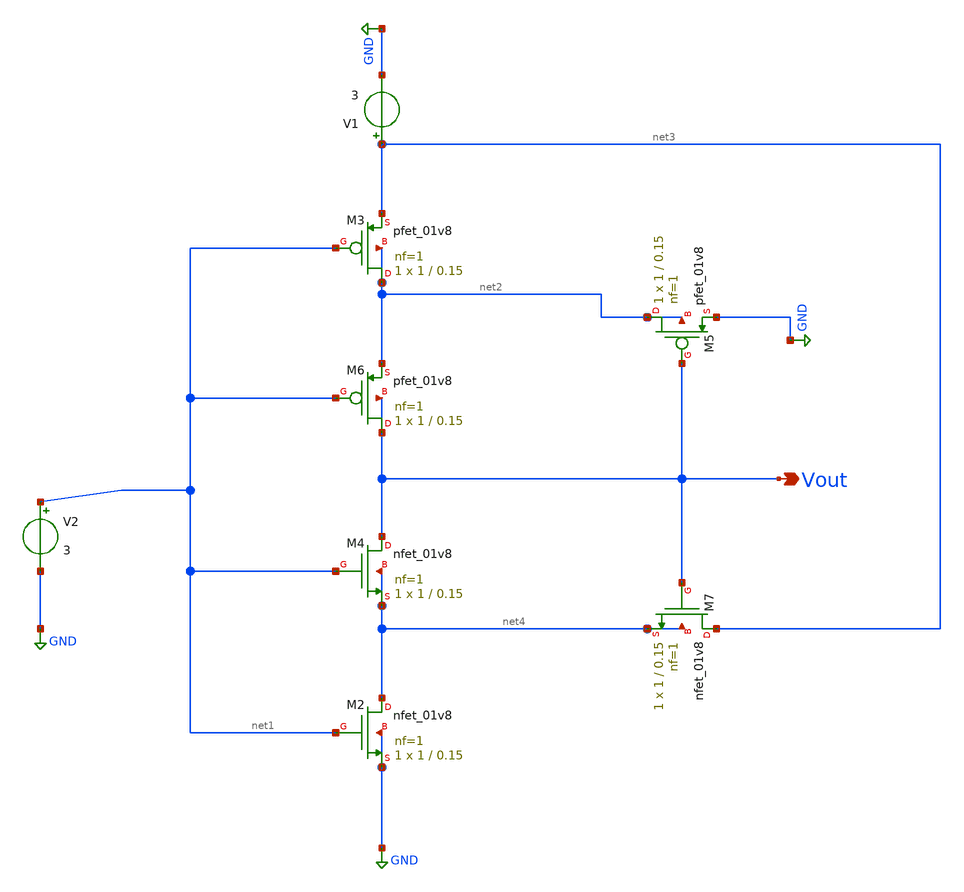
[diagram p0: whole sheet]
** sch_path: Schematics Final/Schmitt Trigger.sch
**.subckt Schmitt Trigger Vout
*.opin Vout
XM2 net4 net1 GND GND sky130_fd_pr__nfet_01v8 L=0.15 W=1 nf=1 ad='int((nf+1)/2) * W/nf * 0.29' as='int((nf+2)/2) * W/nf * 0.29'
+ pd='2*int((nf+1)/2) * (W/nf + 0.29)' ps='2*int((nf+2)/2) * (W/nf + 0.29)' nrd='0.29 / W' nrs='0.29 / W'
+ sa=0 sb=0 sd=0 mult=1 m=1
XM4 Vout net1 net4 net4 sky130_fd_pr__nfet_01v8 L=0.15 W=1 nf=1 ad='int((nf+1)/2) * W/nf * 0.29' as='int((nf+2)/2) * W/nf * 0.29'
+ pd='2*int((nf+1)/2) * (W/nf + 0.29)' ps='2*int((nf+2)/2) * (W/nf + 0.29)' nrd='0.29 / W' nrs='0.29 / W'
+ sa=0 sb=0 sd=0 mult=1 m=1
XM3 net2 net1 net3 net2 sky130_fd_pr__pfet_01v8 L=0.15 W=1 nf=1 ad='int((nf+1)/2) * W/nf * 0.29' as='int((nf+2)/2) * W/nf * 0.29'
+ pd='2*int((nf+1)/2) * (W/nf + 0.29)' ps='2*int((nf+2)/2) * (W/nf + 0.29)' nrd='0.29 / W' nrs='0.29 / W'
+ sa=0 sb=0 sd=0 mult=1 m=1
XM6 Vout net1 net2 Vout sky130_fd_pr__pfet_01v8 L=0.15 W=1 nf=1 ad='int((nf+1)/2) * W/nf * 0.29' as='int((nf+2)/2) * W/nf * 0.29'
+ pd='2*int((nf+1)/2) * (W/nf + 0.29)' ps='2*int((nf+2)/2) * (W/nf + 0.29)' nrd='0.29 / W' nrs='0.29 / W'
+ sa=0 sb=0 sd=0 mult=1 m=1
XM5 net2 Vout GND net2 sky130_fd_pr__pfet_01v8 L=0.15 W=1 nf=1 ad='int((nf+1)/2) * W/nf * 0.29' as='int((nf+2)/2) * W/nf * 0.29'
+ pd='2*int((nf+1)/2) * (W/nf + 0.29)' ps='2*int((nf+2)/2) * (W/nf + 0.29)' nrd='0.29 / W' nrs='0.29 / W'
+ sa=0 sb=0 sd=0 mult=1 m=1
XM7 net3 Vout net4 net4 sky130_fd_pr__nfet_01v8 L=0.15 W=1 nf=1 ad='int((nf+1)/2) * W/nf * 0.29' as='int((nf+2)/2) * W/nf * 0.29'
+ pd='2*int((nf+1)/2) * (W/nf + 0.29)' ps='2*int((nf+2)/2) * (W/nf + 0.29)' nrd='0.29 / W' nrs='0.29 / W'
+ sa=0 sb=0 sd=0 mult=1 m=1
V1 net3 GND 3
V2 net1 GND 3
**.ends
.GLOBAL GND
.end
